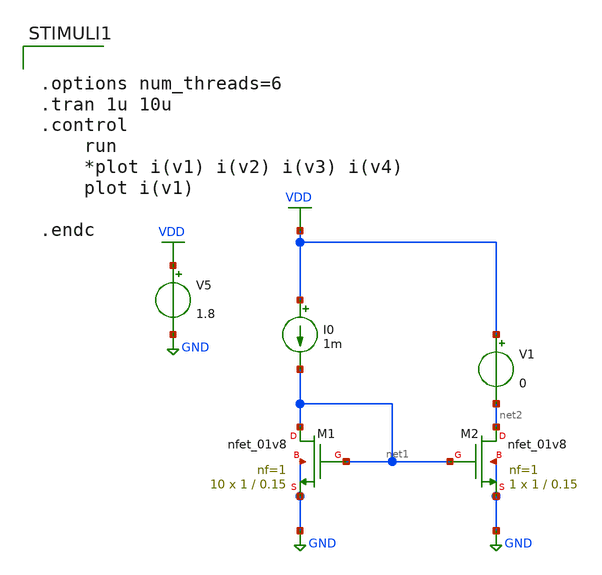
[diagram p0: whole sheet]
** sch_path: Neuron/ultralif/tb_ileak_currmirr.sch
**.subckt tb_ileak_currmirr
XM2 net2 net1 GND GND sky130_fd_pr__nfet_01v8 L=0.15 W=1 nf=1 ad='int((1 + 1)/2) * 1 / 1 * 0.29' as='int((1 + 2)/2) * 1 / 1 * 0.29'
+ pd='2*int((1 + 1)/2) * (1 / 1 + 0.29)' ps='2*int((1 + 2)/2) * (1 / 1 + 0.29)' nrd='0.29 / 1 ' nrs='0.29 / 1 '
+ sa=0 sb=0 sd=0 mult=1 m=1
XM1 net1 net1 GND GND sky130_fd_pr__nfet_01v8 L=0.15 W=1 nf=1 ad='int((1 + 1)/2) * 1 / 1 * 0.29' as='int((1 + 2)/2) * 1 / 1 * 0.29'
+ pd='2*int((1 + 1)/2) * (1 / 1 + 0.29)' ps='2*int((1 + 2)/2) * (1 / 1 + 0.29)' nrd='0.29 / 1 ' nrs='0.29 / 1 '
+ sa=0 sb=0 sd=0 mult=10 m=10
I0 VDD net1 1m
V1 VDD net2 0
V5 VDD GND 1.8
**** begin user architecture code

** opencircuitdesign pdks install
.lib $::SKYWATER_MODELS/sky130.lib.spice tt


**** end user architecture code
**.ends
.GLOBAL GND
.GLOBAL VDD
**** begin user architecture code


.options num_threads=6
.tran 1u 10u
.control
	run
	*plot i(v1) i(v2) i(v3) i(v4)
	plot i(v1)

.endc


**** end user architecture code
.end
